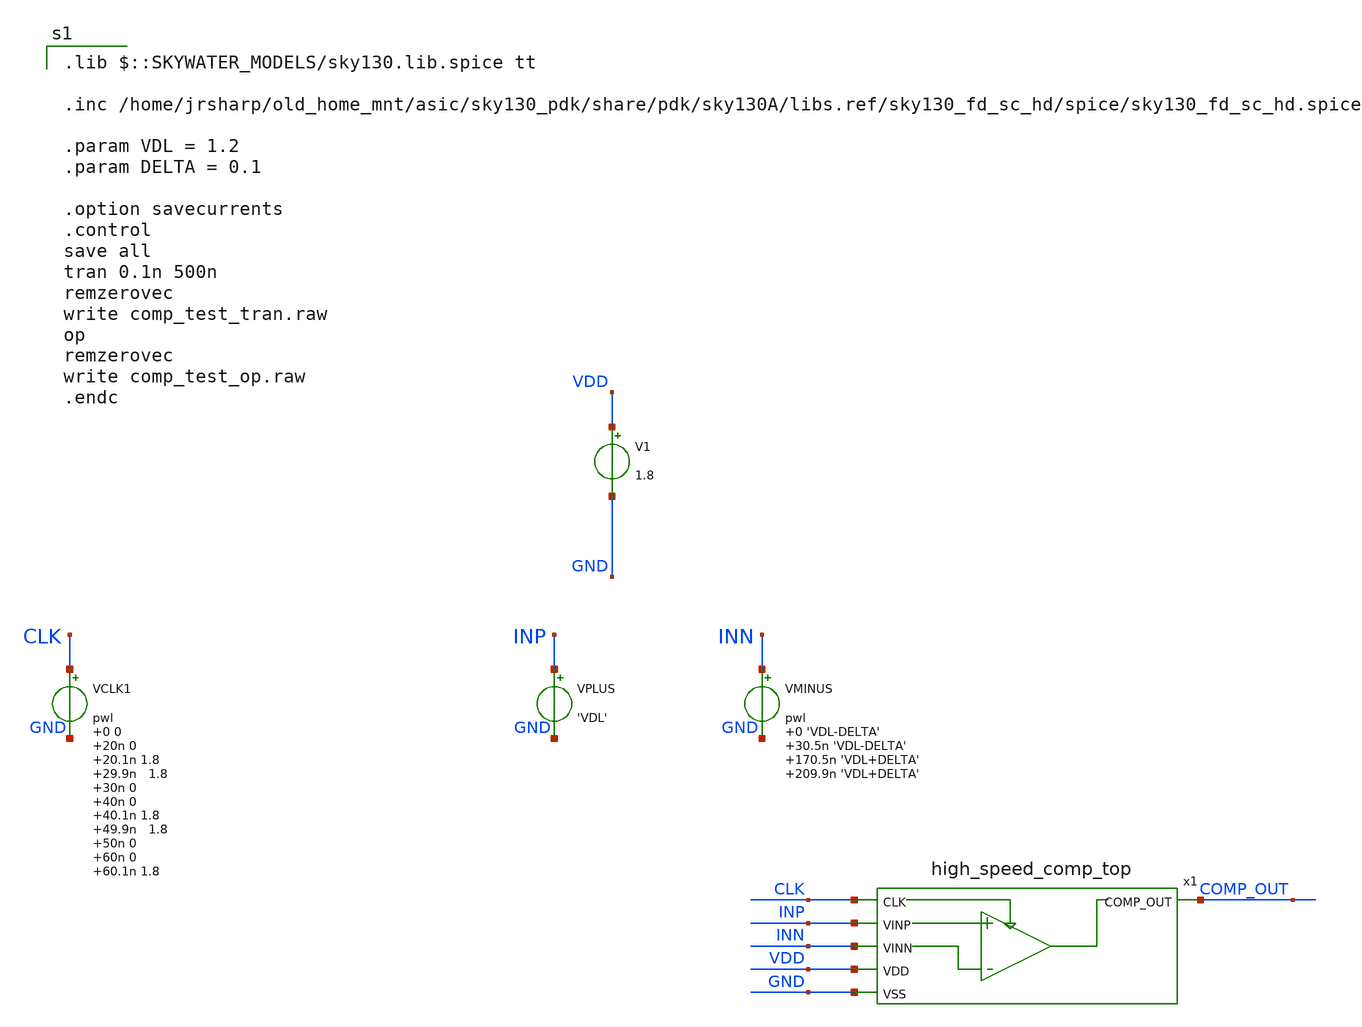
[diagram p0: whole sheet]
** sch_path: xschem/flash_converter/high_speed_comp_test.sch
**.subckt high_speed_comp_test
V1 VDD GND 1.8
VPLUS INP GND 'VDL'
VMINUS INN GND pwl 0 'VDL-DELTA' 30.5n 'VDL-DELTA' 170.5n 'VDL+DELTA' 209.9n 'VDL+DELTA'

VCLK1 CLK GND pwl 0 0 20n 0 20.1n 1.8 29.9n 1.8 30n 0 40n 0 40.1n 1.8 49.9n 1.8 50n 0 60n 0 60.1n
+ 1.8 69.9n 1.8 70n 0 80n 0 80.1n 1.8 89.9n 1.8 90n 0 100n 0 100.1n 1.8 109.9n 1.8 110n 0 120n 0 120.1n
+ 1.8 129.9n 1.8 130n 0 140n 0 140.1n 1.8 149.9n 1.8 150n 0 160n 0 160.1n 1.8 169.9n 1.8 170n 0 180n 0
+ 180.1n 1.8 189.9n 1.8 190n 0 200n 0 200.1n 1.8 209.9n 1.8 210n 0 220n 0 220.1n 1.8 229.9n 1.8 230n 0 240n
+ 0

x1 CLK INP INN VDD COMP_OUT GND high_speed_comp_top
**** begin user architecture code
 .lib $::SKYWATER_MODELS/sky130.lib.spice tt

.inc /home/jrsharp/old_home_mnt/asic/sky130_pdk/share/pdk/sky130A/libs.ref/sky130_fd_sc_hd/spice/sky130_fd_sc_hd.spice

.param VDL = 1.2
.param DELTA = 0.1

.option savecurrents
.control
save all
tran 0.1n 500n
remzerovec
write comp_test_tran.raw
op
remzerovec
write comp_test_op.raw
.endc



**** end user architecture code
**.ends

* expanding   symbol:  high_speed_comp_top.sym # of pins=6
** sym_path: xschem/flash_converter/high_speed_comp_top.sym
** sch_path: xschem/flash_converter/high_speed_comp_top.sch
.subckt high_speed_comp_top CLK VINP VINN VDD COMP_OUT VSS
*.ipin VINP
*.ipin VINN
*.ipin CLK
*.opin COMP_OUT
*.ipin VDD
*.ipin VSS
x1 VDD CLK_PRIME net1 net2 VSS VINP VINN strong_arm_latch
x2 VDD net1 net2 VOUT VSS post_amplifier
x3 CLK VOUT VSS VSS VDD VDD COMP_OUT sky130_fd_sc_hd__dfxtp_2
x4 CLK VSS VSS VDD VDD CLK_PRIME sky130_fd_sc_hd__clkinv_4
x5 VSS VSS VDD VDD sky130_fd_sc_hd__decap_3
x7 VSS VSS VDD VDD sky130_fd_sc_hd__decap_3
x9 VSS VDD sky130_fd_sc_hd__tapvpwrvgnd_1
x6 VSS VDD sky130_fd_sc_hd__tapvpwrvgnd_1
x8 VSS VDD sky130_fd_sc_hd__tapvpwrvgnd_1
.ends


* expanding   symbol:  strong_arm_latch.sym # of pins=7
** sym_path: xschem/flash_converter/strong_arm_latch.sym
** sch_path: xschem/flash_converter/strong_arm_latch.sch
.subckt strong_arm_latch VDD CLK VOUT_PLUS VOUT_MINUS VSS VINP VINN
*.ipin VSS
*.ipin VDD
*.ipin CLK
*.ipin VINP
*.ipin VINN
*.opin VOUT_MINUS
*.opin VOUT_PLUS
XM1 net2 VINP net1 VSS sky130_fd_pr__nfet_01v8_lvt L=1 W=5 nf=1 ad='int((nf+1)/2) * W/nf * 0.29' as='int((nf+2)/2) * W/nf * 0.29'
+ pd='2*int((nf+1)/2) * (W/nf + 0.29)' ps='2*int((nf+2)/2) * (W/nf + 0.29)' nrd='0.29 / W' nrs='0.29 / W'
+ sa=0 sb=0 sd=0 mult=1 m=1
XM2 net3 VINN net1 VSS sky130_fd_pr__nfet_01v8_lvt L=1 W=5 nf=1 ad='int((nf+1)/2) * W/nf * 0.29' as='int((nf+2)/2) * W/nf * 0.29'
+ pd='2*int((nf+1)/2) * (W/nf + 0.29)' ps='2*int((nf+2)/2) * (W/nf + 0.29)' nrd='0.29 / W' nrs='0.29 / W'
+ sa=0 sb=0 sd=0 mult=1 m=1
XM3 net1 CLK VSS VSS sky130_fd_pr__nfet_01v8_lvt L=1 W=5 nf=1 ad='int((nf+1)/2) * W/nf * 0.29' as='int((nf+2)/2) * W/nf * 0.29'
+ pd='2*int((nf+1)/2) * (W/nf + 0.29)' ps='2*int((nf+2)/2) * (W/nf + 0.29)' nrd='0.29 / W' nrs='0.29 / W'
+ sa=0 sb=0 sd=0 mult=1 m=1
XM4 VOUT_PLUS VOUT_MINUS net2 VSS sky130_fd_pr__nfet_01v8 L=0.15 W=1 nf=1 ad='int((nf+1)/2) * W/nf * 0.29'
+ as='int((nf+2)/2) * W/nf * 0.29' pd='2*int((nf+1)/2) * (W/nf + 0.29)' ps='2*int((nf+2)/2) * (W/nf + 0.29)'
+ nrd='0.29 / W' nrs='0.29 / W' sa=0 sb=0 sd=0 mult=1 m=1
XM5 VOUT_MINUS VOUT_PLUS net3 VSS sky130_fd_pr__nfet_01v8 L=0.15 W=1 nf=1 ad='int((nf+1)/2) * W/nf * 0.29'
+ as='int((nf+2)/2) * W/nf * 0.29' pd='2*int((nf+1)/2) * (W/nf + 0.29)' ps='2*int((nf+2)/2) * (W/nf + 0.29)'
+ nrd='0.29 / W' nrs='0.29 / W' sa=0 sb=0 sd=0 mult=1 m=1
XM6 VOUT_PLUS VOUT_MINUS VDD VDD sky130_fd_pr__pfet_01v8 L=0.15 W=1 nf=1 ad='int((nf+1)/2) * W/nf * 0.29'
+ as='int((nf+2)/2) * W/nf * 0.29' pd='2*int((nf+1)/2) * (W/nf + 0.29)' ps='2*int((nf+2)/2) * (W/nf + 0.29)'
+ nrd='0.29 / W' nrs='0.29 / W' sa=0 sb=0 sd=0 mult=1 m=1
XM7 VOUT_MINUS VOUT_PLUS VDD VDD sky130_fd_pr__pfet_01v8 L=0.15 W=1 nf=1 ad='int((nf+1)/2) * W/nf * 0.29'
+ as='int((nf+2)/2) * W/nf * 0.29' pd='2*int((nf+1)/2) * (W/nf + 0.29)' ps='2*int((nf+2)/2) * (W/nf + 0.29)'
+ nrd='0.29 / W' nrs='0.29 / W' sa=0 sb=0 sd=0 mult=1 m=1
XM8 VOUT_PLUS CLK VDD VDD sky130_fd_pr__pfet_01v8 L=0.15 W=10 nf=1 ad='int((nf+1)/2) * W/nf * 0.29' as='int((nf+2)/2) * W/nf * 0.29'
+ pd='2*int((nf+1)/2) * (W/nf + 0.29)' ps='2*int((nf+2)/2) * (W/nf + 0.29)' nrd='0.29 / W' nrs='0.29 / W'
+ sa=0 sb=0 sd=0 mult=1 m=1
XM9 net2 CLK VDD VDD sky130_fd_pr__pfet_01v8 L=0.15 W=10 nf=1 ad='int((nf+1)/2) * W/nf * 0.29' as='int((nf+2)/2) * W/nf * 0.29'
+ pd='2*int((nf+1)/2) * (W/nf + 0.29)' ps='2*int((nf+2)/2) * (W/nf + 0.29)' nrd='0.29 / W' nrs='0.29 / W'
+ sa=0 sb=0 sd=0 mult=1 m=1
XM10 VOUT_MINUS CLK VDD VDD sky130_fd_pr__pfet_01v8 L=0.15 W=10 nf=1 ad='int((nf+1)/2) * W/nf * 0.29'
+ as='int((nf+2)/2) * W/nf * 0.29' pd='2*int((nf+1)/2) * (W/nf + 0.29)' ps='2*int((nf+2)/2) * (W/nf + 0.29)'
+ nrd='0.29 / W' nrs='0.29 / W' sa=0 sb=0 sd=0 mult=1 m=1
XM11 net3 CLK VDD VDD sky130_fd_pr__pfet_01v8 L=0.15 W=10 nf=1 ad='int((nf+1)/2) * W/nf * 0.29' as='int((nf+2)/2) * W/nf * 0.29'
+ pd='2*int((nf+1)/2) * (W/nf + 0.29)' ps='2*int((nf+2)/2) * (W/nf + 0.29)' nrd='0.29 / W' nrs='0.29 / W'
+ sa=0 sb=0 sd=0 mult=1 m=1
.ends


* expanding   symbol:  post_amplifier.sym # of pins=5
** sym_path: xschem/flash_converter/post_amplifier.sym
** sch_path: xschem/flash_converter/post_amplifier.sch
.subckt post_amplifier VDD VLAT_PLUS VLAT_MINUS VOUT VSS
*.ipin VLAT_PLUS
*.ipin VLAT_MINUS
*.ipin VDD
*.ipin VSS
*.opin VOUT
XM1 net1 VLAT_PLUS net4 VSS sky130_fd_pr__nfet_01v8 L=0.15 W=1 nf=1 ad='int((nf+1)/2) * W/nf * 0.29'
+ as='int((nf+2)/2) * W/nf * 0.29' pd='2*int((nf+1)/2) * (W/nf + 0.29)' ps='2*int((nf+2)/2) * (W/nf + 0.29)'
+ nrd='0.29 / W' nrs='0.29 / W' sa=0 sb=0 sd=0 mult=1 m=1
XM2 net3 VLAT_MINUS net4 VSS sky130_fd_pr__nfet_01v8 L=0.15 W=1 nf=1 ad='int((nf+1)/2) * W/nf * 0.29'
+ as='int((nf+2)/2) * W/nf * 0.29' pd='2*int((nf+1)/2) * (W/nf + 0.29)' ps='2*int((nf+2)/2) * (W/nf + 0.29)'
+ nrd='0.29 / W' nrs='0.29 / W' sa=0 sb=0 sd=0 mult=1 m=1
XM3 net4 net1 VSS VSS sky130_fd_pr__nfet_01v8 L=0.15 W=1 nf=1 ad='int((nf+1)/2) * W/nf * 0.29' as='int((nf+2)/2) * W/nf * 0.29'
+ pd='2*int((nf+1)/2) * (W/nf + 0.29)' ps='2*int((nf+2)/2) * (W/nf + 0.29)' nrd='0.29 / W' nrs='0.29 / W'
+ sa=0 sb=0 sd=0 mult=1 m=1
XM4 net1 VLAT_PLUS net2 VDD sky130_fd_pr__pfet_01v8 L=0.15 W=1 nf=1 ad='int((nf+1)/2) * W/nf * 0.29'
+ as='int((nf+2)/2) * W/nf * 0.29' pd='2*int((nf+1)/2) * (W/nf + 0.29)' ps='2*int((nf+2)/2) * (W/nf + 0.29)'
+ nrd='0.29 / W' nrs='0.29 / W' sa=0 sb=0 sd=0 mult=1 m=1
XM5 net3 VLAT_MINUS net2 VDD sky130_fd_pr__pfet_01v8 L=0.15 W=1 nf=1 ad='int((nf+1)/2) * W/nf * 0.29'
+ as='int((nf+2)/2) * W/nf * 0.29' pd='2*int((nf+1)/2) * (W/nf + 0.29)' ps='2*int((nf+2)/2) * (W/nf + 0.29)'
+ nrd='0.29 / W' nrs='0.29 / W' sa=0 sb=0 sd=0 mult=1 m=1
XM6 net2 net1 VDD VDD sky130_fd_pr__pfet_01v8 L=0.15 W=1 nf=1 ad='int((nf+1)/2) * W/nf * 0.29' as='int((nf+2)/2) * W/nf * 0.29'
+ pd='2*int((nf+1)/2) * (W/nf + 0.29)' ps='2*int((nf+2)/2) * (W/nf + 0.29)' nrd='0.29 / W' nrs='0.29 / W'
+ sa=0 sb=0 sd=0 mult=1 m=1
XM7 VOUT net3 VSS VSS sky130_fd_pr__nfet_01v8 L=0.15 W=1 nf=1 ad='int((nf+1)/2) * W/nf * 0.29' as='int((nf+2)/2) * W/nf * 0.29'
+ pd='2*int((nf+1)/2) * (W/nf + 0.29)' ps='2*int((nf+2)/2) * (W/nf + 0.29)' nrd='0.29 / W' nrs='0.29 / W'
+ sa=0 sb=0 sd=0 mult=1 m=1
XM8 VOUT net3 VDD VDD sky130_fd_pr__pfet_01v8 L=0.15 W=1 nf=1 ad='int((nf+1)/2) * W/nf * 0.29' as='int((nf+2)/2) * W/nf * 0.29'
+ pd='2*int((nf+1)/2) * (W/nf + 0.29)' ps='2*int((nf+2)/2) * (W/nf + 0.29)' nrd='0.29 / W' nrs='0.29 / W'
+ sa=0 sb=0 sd=0 mult=1 m=1
.ends

.end
